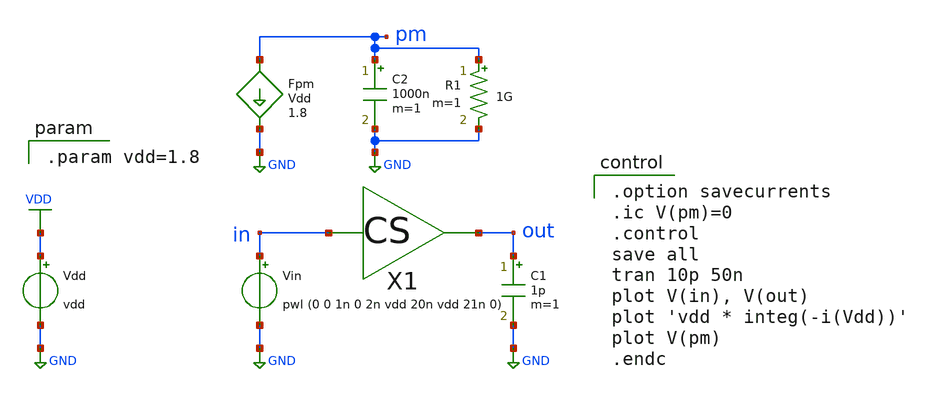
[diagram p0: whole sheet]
** sch_path: xschem/tb/tran_03_pm.sch
**.subckt tran_03_pm
Vdd VDD GND vdd
Vin in GND pwl (0 0 1n 0 2n vdd 20n vdd 21n 0)
X1 in out cs
C1 out GND 1p m=1
Fpm pm GND Vdd 1.8
C2 pm GND 1000n m=1
R1 pm GND 1G m=1
**** begin user architecture code

.model nch nmos ( version=4.7 level=54 lmin=0.1u lmax=20u wmin=0.1u wmax=10u  )
.model pch pmos ( version=4.7 level=54 lmin=0.1u lmax=20u wmin=0.1u wmax=10u  )


.option savecurrents
.ic V(pm)=0
.control
save all
tran 10p 50n
plot V(in), V(out)
plot 'vdd * integ(-i(Vdd))'
plot V(pm)
.endc


.param vdd=1.8

**** end user architecture code
**.ends

* expanding   symbol:  cs.sym # of pins=2
** sym_path: xschem/tb/cs.sym
** sch_path: xschem/tb/cs.sch
.subckt cs in out
*.ipin in
*.opin out
R1 VDD out 1k m=1
M1 out in GND GND nch w=3.6u l=0.18u m=1
.ends

.GLOBAL VDD
.GLOBAL GND
.end
